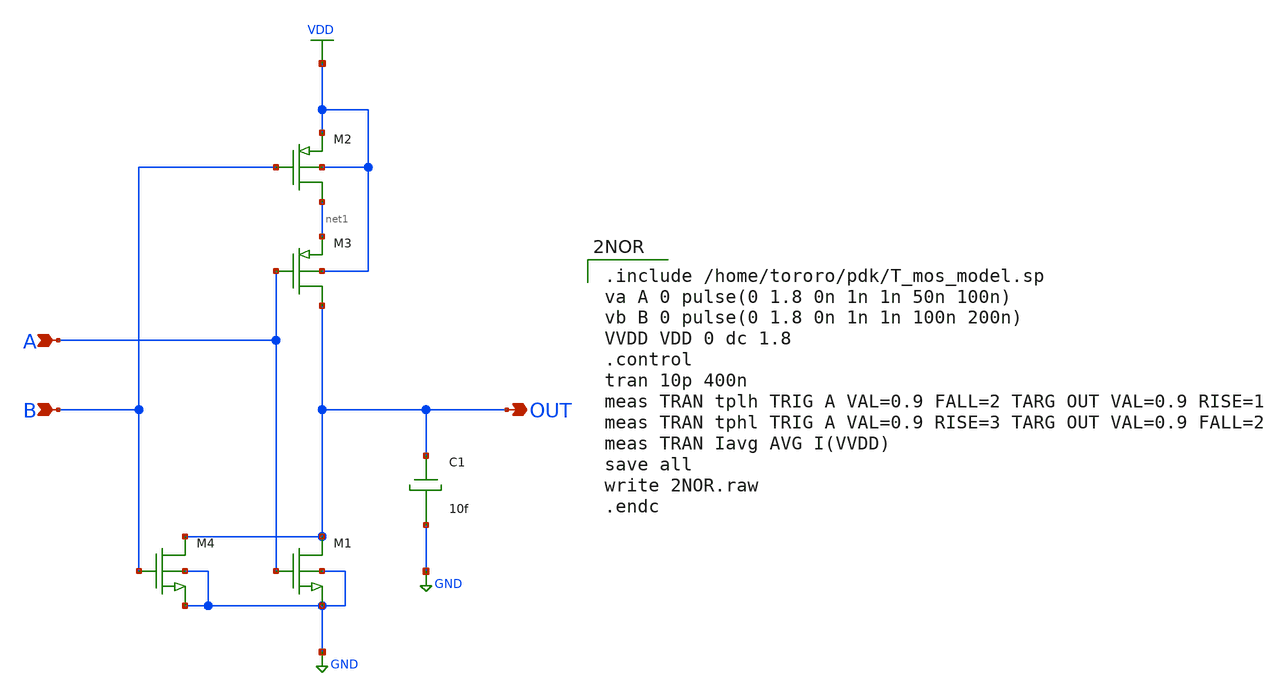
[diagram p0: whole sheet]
** sch_path: task1/2NOR.sch
**.subckt 2NOR OUT B A
*.opin OUT
*.ipin B
*.ipin A
M1 OUT A GND GND nch w=3.5u l=0.35u as=0 ps=0 ad=0 pd=0 m=1
M2 net1 B VDD VDD pch w=3.5u l=0.35u as=0 ps=0 ad=0 pd=0 m=1
M3 OUT A net1 VDD pch w=3.5u l=0.35u as=0 ps=0 ad=0 pd=0 m=1
M4 OUT B GND GND nch w=3.5u l=0.35u as=0 ps=0 ad=0 pd=0 m=1
C1 OUT GND 10f m=1
**** begin user architecture code

.include /home/tororo/pdk/T_mos_model.sp
va A 0 pulse(0 1.8 0n 1n 1n 50n 100n)
vb B 0 pulse(0 1.8 0n 1n 1n 100n 200n)
VVDD VDD 0 dc 1.8
.control
tran 10p 400n
meas TRAN tplh TRIG A VAL=0.9 FALL=2 TARG OUT VAL=0.9 RISE=1
meas TRAN tphl TRIG A VAL=0.9 RISE=3 TARG OUT VAL=0.9 FALL=2
meas TRAN Iavg AVG I(VVDD)
save all
write 2NOR.raw
.endc

**** end user architecture code
**.ends
.GLOBAL VDD
.GLOBAL GND
.end
